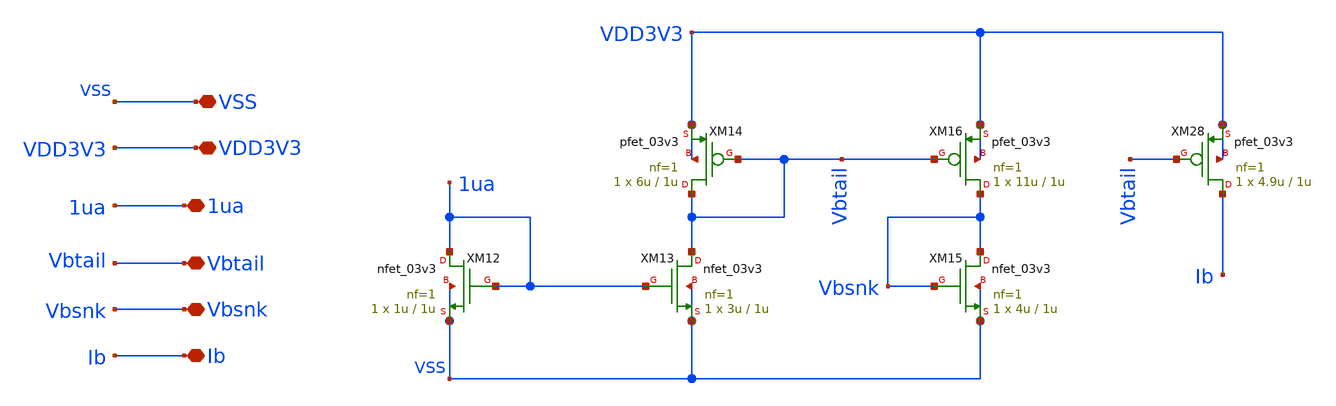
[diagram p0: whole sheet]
** sch_path: designs/libs/core_pga/folded_cascode/bias.sch
**.subckt bias VSS VDD3V3 1ua Vbtail Vbsnk Ib
*.iopin VSS
*.iopin VDD3V3
*.iopin 1ua
*.iopin Vbtail
*.iopin Vbsnk
*.iopin Ib
XM12 1ua 1ua VSS VSS nfet_03v3 L=1u W=1u nf=1 ad='int((nf+1)/2) * W/nf * 0.18u' as='int((nf+2)/2) * W/nf * 0.18u'
+ pd='2*int((nf+1)/2) * (W/nf + 0.18u)' ps='2*int((nf+2)/2) * (W/nf + 0.18u)' nrd='0.18u / W' nrs='0.18u / W'
+ sa=0 sb=0 sd=0 m=1
XM13 Vbtail 1ua VSS VSS nfet_03v3 L=1u W=3u nf=1 ad='int((nf+1)/2) * W/nf * 0.18u' as='int((nf+2)/2) * W/nf * 0.18u'
+ pd='2*int((nf+1)/2) * (W/nf + 0.18u)' ps='2*int((nf+2)/2) * (W/nf + 0.18u)' nrd='0.18u / W' nrs='0.18u / W'
+ sa=0 sb=0 sd=0 m=1
XM14 Vbtail Vbtail VDD3V3 VDD3V3 pfet_03v3 L=1u W=6u nf=1 ad='int((nf+1)/2) * W/nf * 0.18u' as='int((nf+2)/2) * W/nf * 0.18u'
+ pd='2*int((nf+1)/2) * (W/nf + 0.18u)' ps='2*int((nf+2)/2) * (W/nf + 0.18u)' nrd='0.18u / W' nrs='0.18u / W'
+ sa=0 sb=0 sd=0 m=1
XM15 Vbsnk Vbsnk VSS VSS nfet_03v3 L=1u W=4u nf=1 ad='int((nf+1)/2) * W/nf * 0.18u' as='int((nf+2)/2) * W/nf * 0.18u'
+ pd='2*int((nf+1)/2) * (W/nf + 0.18u)' ps='2*int((nf+2)/2) * (W/nf + 0.18u)' nrd='0.18u / W' nrs='0.18u / W'
+ sa=0 sb=0 sd=0 m=1
XM16 Vbsnk Vbtail VDD3V3 VDD3V3 pfet_03v3 L=1u W=11u nf=1 ad='int((nf+1)/2) * W/nf * 0.18u' as='int((nf+2)/2) * W/nf * 0.18u'
+ pd='2*int((nf+1)/2) * (W/nf + 0.18u)' ps='2*int((nf+2)/2) * (W/nf + 0.18u)' nrd='0.18u / W' nrs='0.18u / W'
+ sa=0 sb=0 sd=0 m=1
XM28 Ib Vbtail VDD3V3 VDD3V3 pfet_03v3 L=1u W=4.9u nf=1 ad='int((nf+1)/2) * W/nf * 0.18u' as='int((nf+2)/2) * W/nf * 0.18u'
+ pd='2*int((nf+1)/2) * (W/nf + 0.18u)' ps='2*int((nf+2)/2) * (W/nf + 0.18u)' nrd='0.18u / W' nrs='0.18u / W'
+ sa=0 sb=0 sd=0 m=1
**.ends
.end
